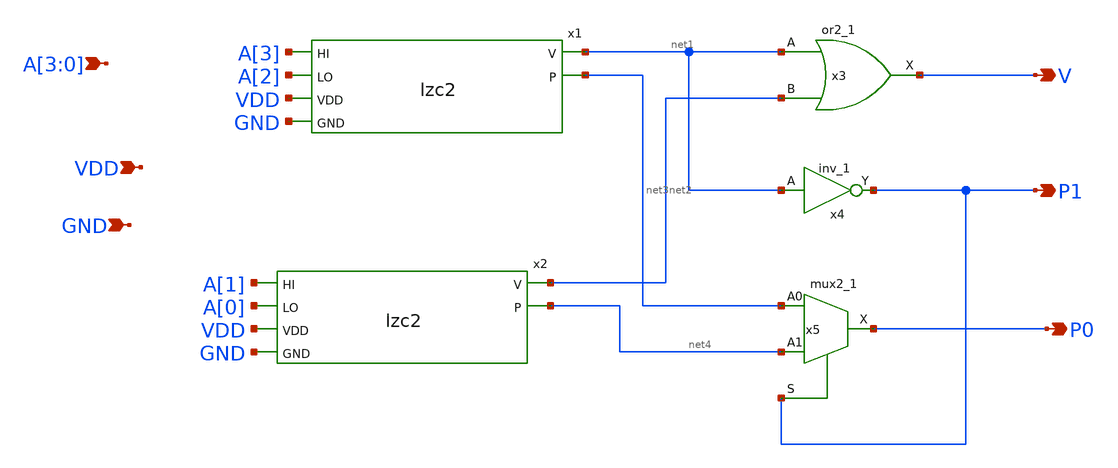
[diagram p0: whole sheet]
** sch_path: frontend/xschem/lzc4.sch
**.subckt lzc4 A[3],A[2],A[1],A[0] V P1 P0 VDD GND
*.ipin A[3],A[2],A[1],A[0]
*.opin V
*.opin P1
*.opin P0
*.ipin VDD
*.ipin GND
x1 A[3] net1 A[2] VDD net3 GND lzc2
x2 A[1] net2 A[0] VDD net4 GND lzc2
x3 net1 net2 GND GND VDD VDD V sky130_fd_sc_hd__or2_1
x4 net1 GND GND VDD VDD P1 sky130_fd_sc_hd__inv_1
x5 net3 net4 P1 GND GND VDD VDD P0 sky130_fd_sc_hd__mux2_1
**.ends

* expanding   symbol:  lzc2.sym # of pins=6
** sym_path: frontend/xschem/lzc2.sym
** sch_path: frontend/xschem/lzc2.sch
.subckt lzc2 HI V LO VDD P GND
*.ipin HI
*.ipin LO
*.opin V
*.opin P
*.ipin VDD
*.ipin GND
x1 HI LO GND GND VDD VDD V sky130_fd_sc_hd__or2_1
x2 HI GND GND VDD VDD P sky130_fd_sc_hd__inv_1
.ends

.end
